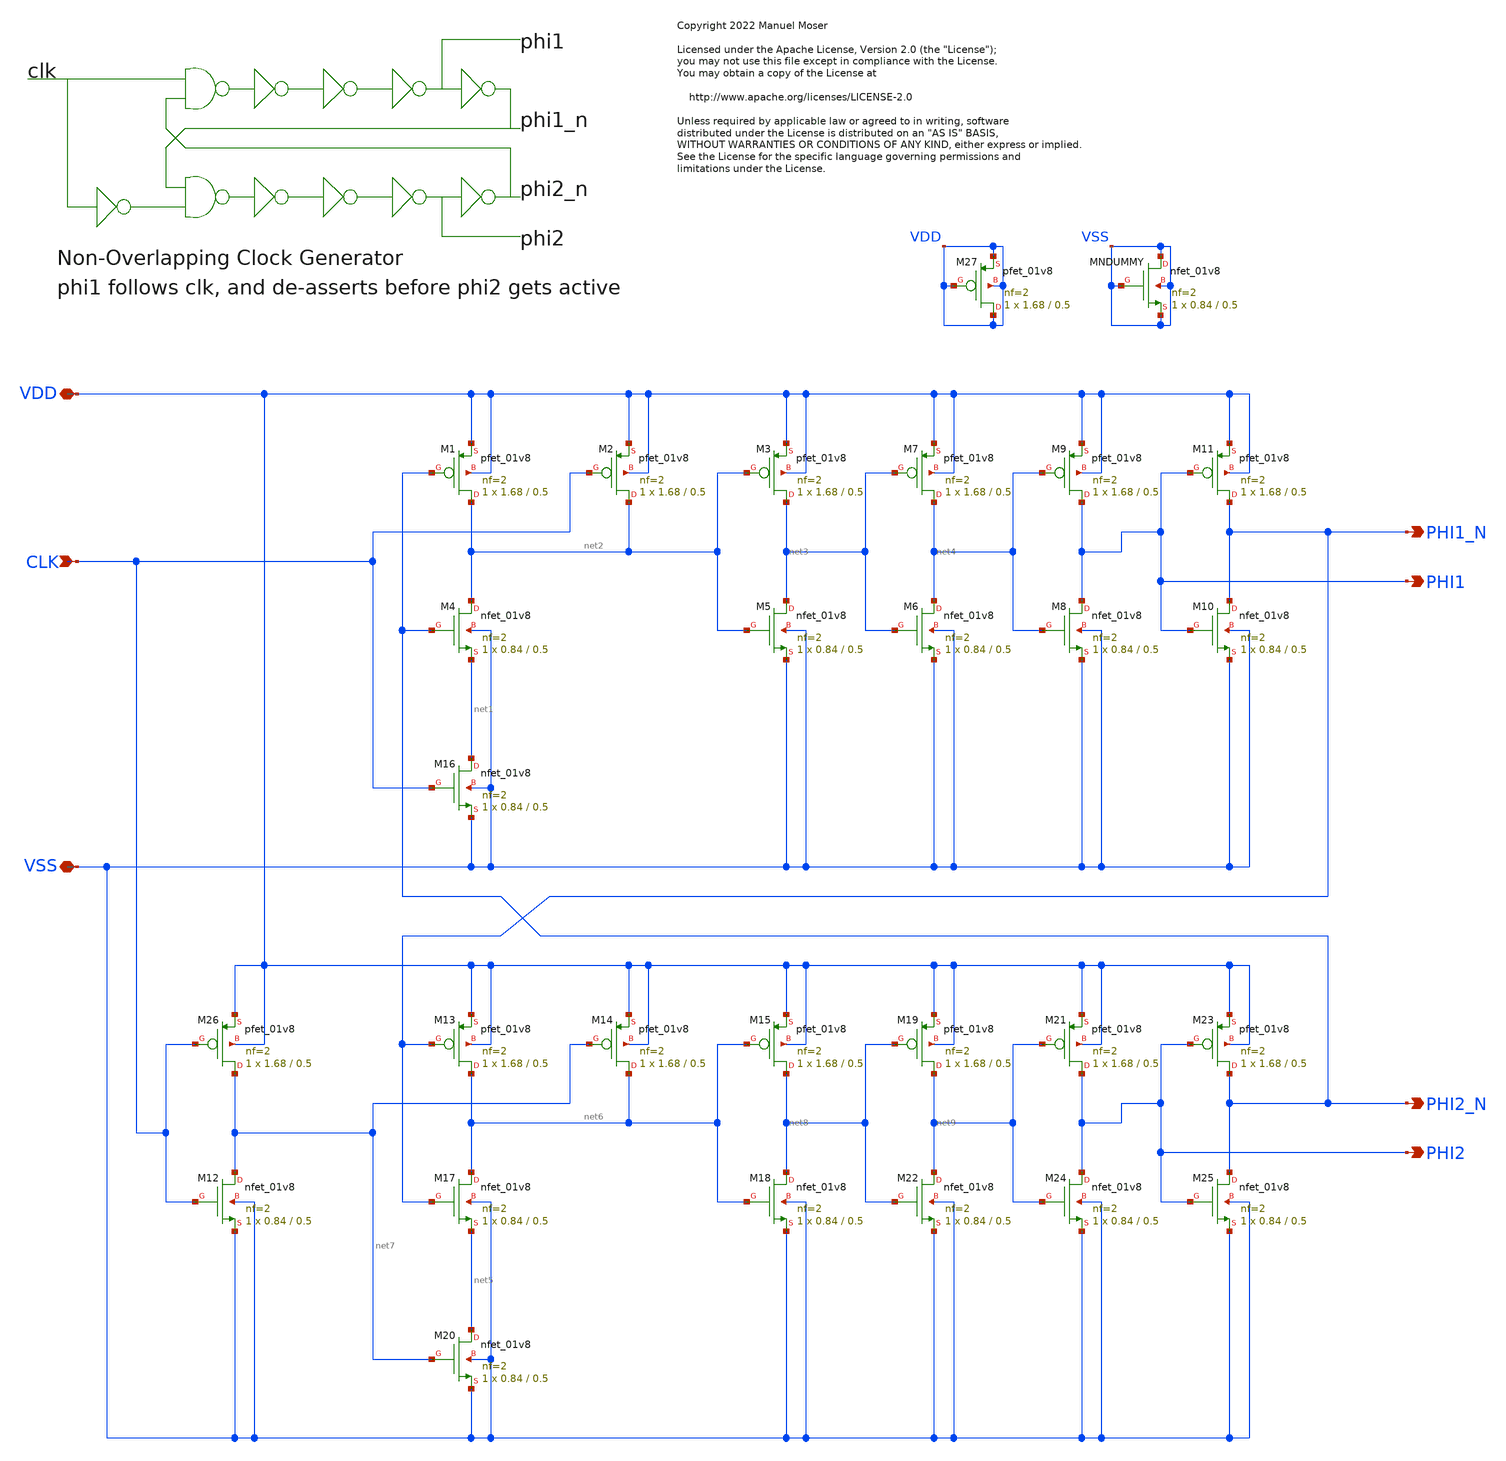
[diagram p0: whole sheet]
** sch_path: xschem/adc_cm_clkgen/adc_cm_clkgen.sch
* Copyright 2022 Manuel Moser
* Licensed under the Apache License, Version 2.0 (the "License");
**.subckt adc_cm_clkgen VDD VSS CLK PHI2_N PHI2 PHI1 PHI1_N
*.iopin VDD
*.iopin VSS
*.ipin CLK
*.opin PHI2_N
*.opin PHI2
*.opin PHI1
*.opin PHI1_N
XM1 net2 PHI2_N VDD VDD sky130_fd_pr__pfet_01v8 L=0.5 W=1.68 nf=2 ad='int((nf+1)/2) * W/nf * 0.29' as='int((nf+2)/2) * W/nf * 0.29'
+ pd='2*int((nf+1)/2) * (W/nf + 0.29)' ps='2*int((nf+2)/2) * (W/nf + 0.29)' nrd='0.29 / W' nrs='0.29 / W'
+ sa=0 sb=0 sd=0 mult=1 m=1
XM2 net2 CLK VDD VDD sky130_fd_pr__pfet_01v8 L=0.5 W=1.68 nf=2 ad='int((nf+1)/2) * W/nf * 0.29' as='int((nf+2)/2) * W/nf * 0.29'
+ pd='2*int((nf+1)/2) * (W/nf + 0.29)' ps='2*int((nf+2)/2) * (W/nf + 0.29)' nrd='0.29 / W' nrs='0.29 / W'
+ sa=0 sb=0 sd=0 mult=1 m=1
XM3 net3 net2 VDD VDD sky130_fd_pr__pfet_01v8 L=0.5 W=1.68 nf=2 ad='int((nf+1)/2) * W/nf * 0.29' as='int((nf+2)/2) * W/nf * 0.29'
+ pd='2*int((nf+1)/2) * (W/nf + 0.29)' ps='2*int((nf+2)/2) * (W/nf + 0.29)' nrd='0.29 / W' nrs='0.29 / W'
+ sa=0 sb=0 sd=0 mult=1 m=1
XM7 net4 net3 VDD VDD sky130_fd_pr__pfet_01v8 L=0.5 W=1.68 nf=2 ad='int((nf+1)/2) * W/nf * 0.29' as='int((nf+2)/2) * W/nf * 0.29'
+ pd='2*int((nf+1)/2) * (W/nf + 0.29)' ps='2*int((nf+2)/2) * (W/nf + 0.29)' nrd='0.29 / W' nrs='0.29 / W'
+ sa=0 sb=0 sd=0 mult=1 m=1
XM9 PHI1 net4 VDD VDD sky130_fd_pr__pfet_01v8 L=0.5 W=1.68 nf=2 ad='int((nf+1)/2) * W/nf * 0.29' as='int((nf+2)/2) * W/nf * 0.29'
+ pd='2*int((nf+1)/2) * (W/nf + 0.29)' ps='2*int((nf+2)/2) * (W/nf + 0.29)' nrd='0.29 / W' nrs='0.29 / W'
+ sa=0 sb=0 sd=0 mult=1 m=1
XM11 PHI1_N PHI1 VDD VDD sky130_fd_pr__pfet_01v8 L=0.5 W=1.68 nf=2 ad='int((nf+1)/2) * W/nf * 0.29' as='int((nf+2)/2) * W/nf * 0.29'
+ pd='2*int((nf+1)/2) * (W/nf + 0.29)' ps='2*int((nf+2)/2) * (W/nf + 0.29)' nrd='0.29 / W' nrs='0.29 / W'
+ sa=0 sb=0 sd=0 mult=1 m=1
XM13 net6 PHI1_N VDD VDD sky130_fd_pr__pfet_01v8 L=0.5 W=1.68 nf=2 ad='int((nf+1)/2) * W/nf * 0.29' as='int((nf+2)/2) * W/nf * 0.29'
+ pd='2*int((nf+1)/2) * (W/nf + 0.29)' ps='2*int((nf+2)/2) * (W/nf + 0.29)' nrd='0.29 / W' nrs='0.29 / W'
+ sa=0 sb=0 sd=0 mult=1 m=1
XM14 net6 net7 VDD VDD sky130_fd_pr__pfet_01v8 L=0.5 W=1.68 nf=2 ad='int((nf+1)/2) * W/nf * 0.29' as='int((nf+2)/2) * W/nf * 0.29'
+ pd='2*int((nf+1)/2) * (W/nf + 0.29)' ps='2*int((nf+2)/2) * (W/nf + 0.29)' nrd='0.29 / W' nrs='0.29 / W'
+ sa=0 sb=0 sd=0 mult=1 m=1
XM15 net8 net6 VDD VDD sky130_fd_pr__pfet_01v8 L=0.5 W=1.68 nf=2 ad='int((nf+1)/2) * W/nf * 0.29' as='int((nf+2)/2) * W/nf * 0.29'
+ pd='2*int((nf+1)/2) * (W/nf + 0.29)' ps='2*int((nf+2)/2) * (W/nf + 0.29)' nrd='0.29 / W' nrs='0.29 / W'
+ sa=0 sb=0 sd=0 mult=1 m=1
XM19 net9 net8 VDD VDD sky130_fd_pr__pfet_01v8 L=0.5 W=1.68 nf=2 ad='int((nf+1)/2) * W/nf * 0.29' as='int((nf+2)/2) * W/nf * 0.29'
+ pd='2*int((nf+1)/2) * (W/nf + 0.29)' ps='2*int((nf+2)/2) * (W/nf + 0.29)' nrd='0.29 / W' nrs='0.29 / W'
+ sa=0 sb=0 sd=0 mult=1 m=1
XM21 PHI2 net9 VDD VDD sky130_fd_pr__pfet_01v8 L=0.5 W=1.68 nf=2 ad='int((nf+1)/2) * W/nf * 0.29' as='int((nf+2)/2) * W/nf * 0.29'
+ pd='2*int((nf+1)/2) * (W/nf + 0.29)' ps='2*int((nf+2)/2) * (W/nf + 0.29)' nrd='0.29 / W' nrs='0.29 / W'
+ sa=0 sb=0 sd=0 mult=1 m=1
XM23 PHI2_N PHI2 VDD VDD sky130_fd_pr__pfet_01v8 L=0.5 W=1.68 nf=2 ad='int((nf+1)/2) * W/nf * 0.29' as='int((nf+2)/2) * W/nf * 0.29'
+ pd='2*int((nf+1)/2) * (W/nf + 0.29)' ps='2*int((nf+2)/2) * (W/nf + 0.29)' nrd='0.29 / W' nrs='0.29 / W'
+ sa=0 sb=0 sd=0 mult=1 m=1
XM26 net7 CLK VDD VDD sky130_fd_pr__pfet_01v8 L=0.5 W=1.68 nf=2 ad='int((nf+1)/2) * W/nf * 0.29' as='int((nf+2)/2) * W/nf * 0.29'
+ pd='2*int((nf+1)/2) * (W/nf + 0.29)' ps='2*int((nf+2)/2) * (W/nf + 0.29)' nrd='0.29 / W' nrs='0.29 / W'
+ sa=0 sb=0 sd=0 mult=1 m=1
XM4 net2 PHI2_N net1 VSS sky130_fd_pr__nfet_01v8 L=0.5 W=0.84 nf=2 ad='int((nf+1)/2) * W/nf * 0.29' as='int((nf+2)/2) * W/nf * 0.29'
+ pd='2*int((nf+1)/2) * (W/nf + 0.29)' ps='2*int((nf+2)/2) * (W/nf + 0.29)' nrd='0.29 / W' nrs='0.29 / W'
+ sa=0 sb=0 sd=0 mult=1 m=1
XM5 net3 net2 VSS VSS sky130_fd_pr__nfet_01v8 L=0.5 W=0.84 nf=2 ad='int((nf+1)/2) * W/nf * 0.29' as='int((nf+2)/2) * W/nf * 0.29'
+ pd='2*int((nf+1)/2) * (W/nf + 0.29)' ps='2*int((nf+2)/2) * (W/nf + 0.29)' nrd='0.29 / W' nrs='0.29 / W'
+ sa=0 sb=0 sd=0 mult=1 m=1
XM6 net4 net3 VSS VSS sky130_fd_pr__nfet_01v8 L=0.5 W=0.84 nf=2 ad='int((nf+1)/2) * W/nf * 0.29' as='int((nf+2)/2) * W/nf * 0.29'
+ pd='2*int((nf+1)/2) * (W/nf + 0.29)' ps='2*int((nf+2)/2) * (W/nf + 0.29)' nrd='0.29 / W' nrs='0.29 / W'
+ sa=0 sb=0 sd=0 mult=1 m=1
XM8 PHI1 net4 VSS VSS sky130_fd_pr__nfet_01v8 L=0.5 W=0.84 nf=2 ad='int((nf+1)/2) * W/nf * 0.29' as='int((nf+2)/2) * W/nf * 0.29'
+ pd='2*int((nf+1)/2) * (W/nf + 0.29)' ps='2*int((nf+2)/2) * (W/nf + 0.29)' nrd='0.29 / W' nrs='0.29 / W'
+ sa=0 sb=0 sd=0 mult=1 m=1
XM10 PHI1_N PHI1 VSS VSS sky130_fd_pr__nfet_01v8 L=0.5 W=0.84 nf=2 ad='int((nf+1)/2) * W/nf * 0.29' as='int((nf+2)/2) * W/nf * 0.29'
+ pd='2*int((nf+1)/2) * (W/nf + 0.29)' ps='2*int((nf+2)/2) * (W/nf + 0.29)' nrd='0.29 / W' nrs='0.29 / W'
+ sa=0 sb=0 sd=0 mult=1 m=1
XM12 net7 CLK VSS VSS sky130_fd_pr__nfet_01v8 L=0.5 W=0.84 nf=2 ad='int((nf+1)/2) * W/nf * 0.29' as='int((nf+2)/2) * W/nf * 0.29'
+ pd='2*int((nf+1)/2) * (W/nf + 0.29)' ps='2*int((nf+2)/2) * (W/nf + 0.29)' nrd='0.29 / W' nrs='0.29 / W'
+ sa=0 sb=0 sd=0 mult=1 m=1
XM16 net1 CLK VSS VSS sky130_fd_pr__nfet_01v8 L=0.5 W=0.84 nf=2 ad='int((nf+1)/2) * W/nf * 0.29' as='int((nf+2)/2) * W/nf * 0.29'
+ pd='2*int((nf+1)/2) * (W/nf + 0.29)' ps='2*int((nf+2)/2) * (W/nf + 0.29)' nrd='0.29 / W' nrs='0.29 / W'
+ sa=0 sb=0 sd=0 mult=1 m=1
XM17 net6 PHI1_N net5 VSS sky130_fd_pr__nfet_01v8 L=0.5 W=0.84 nf=2 ad='int((nf+1)/2) * W/nf * 0.29'
+ as='int((nf+2)/2) * W/nf * 0.29' pd='2*int((nf+1)/2) * (W/nf + 0.29)' ps='2*int((nf+2)/2) * (W/nf + 0.29)'
+ nrd='0.29 / W' nrs='0.29 / W' sa=0 sb=0 sd=0 mult=1 m=1
XM18 net8 net6 VSS VSS sky130_fd_pr__nfet_01v8 L=0.5 W=0.84 nf=2 ad='int((nf+1)/2) * W/nf * 0.29' as='int((nf+2)/2) * W/nf * 0.29'
+ pd='2*int((nf+1)/2) * (W/nf + 0.29)' ps='2*int((nf+2)/2) * (W/nf + 0.29)' nrd='0.29 / W' nrs='0.29 / W'
+ sa=0 sb=0 sd=0 mult=1 m=1
XM20 net5 net7 VSS VSS sky130_fd_pr__nfet_01v8 L=0.5 W=0.84 nf=2 ad='int((nf+1)/2) * W/nf * 0.29' as='int((nf+2)/2) * W/nf * 0.29'
+ pd='2*int((nf+1)/2) * (W/nf + 0.29)' ps='2*int((nf+2)/2) * (W/nf + 0.29)' nrd='0.29 / W' nrs='0.29 / W'
+ sa=0 sb=0 sd=0 mult=1 m=1
XM22 net9 net8 VSS VSS sky130_fd_pr__nfet_01v8 L=0.5 W=0.84 nf=2 ad='int((nf+1)/2) * W/nf * 0.29' as='int((nf+2)/2) * W/nf * 0.29'
+ pd='2*int((nf+1)/2) * (W/nf + 0.29)' ps='2*int((nf+2)/2) * (W/nf + 0.29)' nrd='0.29 / W' nrs='0.29 / W'
+ sa=0 sb=0 sd=0 mult=1 m=1
XM24 PHI2 net9 VSS VSS sky130_fd_pr__nfet_01v8 L=0.5 W=0.84 nf=2 ad='int((nf+1)/2) * W/nf * 0.29' as='int((nf+2)/2) * W/nf * 0.29'
+ pd='2*int((nf+1)/2) * (W/nf + 0.29)' ps='2*int((nf+2)/2) * (W/nf + 0.29)' nrd='0.29 / W' nrs='0.29 / W'
+ sa=0 sb=0 sd=0 mult=1 m=1
XM25 PHI2_N PHI2 VSS VSS sky130_fd_pr__nfet_01v8 L=0.5 W=0.84 nf=2 ad='int((nf+1)/2) * W/nf * 0.29' as='int((nf+2)/2) * W/nf * 0.29'
+ pd='2*int((nf+1)/2) * (W/nf + 0.29)' ps='2*int((nf+2)/2) * (W/nf + 0.29)' nrd='0.29 / W' nrs='0.29 / W'
+ sa=0 sb=0 sd=0 mult=1 m=1
XM27 VDD VDD VDD VDD sky130_fd_pr__pfet_01v8 L=0.5 W=1.68 nf=2 ad='int((nf+1)/2) * W/nf * 0.29' as='int((nf+2)/2) * W/nf * 0.29'
+ pd='2*int((nf+1)/2) * (W/nf + 0.29)' ps='2*int((nf+2)/2) * (W/nf + 0.29)' nrd='0.29 / W' nrs='0.29 / W'
+ sa=0 sb=0 sd=0 mult=1 m=1
XMNDUMMY VSS VSS VSS VSS sky130_fd_pr__nfet_01v8 L=0.5 W=0.84 nf=2 ad='int((nf+1)/2) * W/nf * 0.29' as='int((nf+2)/2) * W/nf * 0.29'
+ pd='2*int((nf+1)/2) * (W/nf + 0.29)' ps='2*int((nf+2)/2) * (W/nf + 0.29)' nrd='0.29 / W' nrs='0.29 / W'
+ sa=0 sb=0 sd=0 mult=1 m=1
**** begin user architecture code

** opencircuitdesign pdks install
.lib $::SKYWATER_MODELS/sky130.lib.spice tt


**** end user architecture code
**.ends
.end
